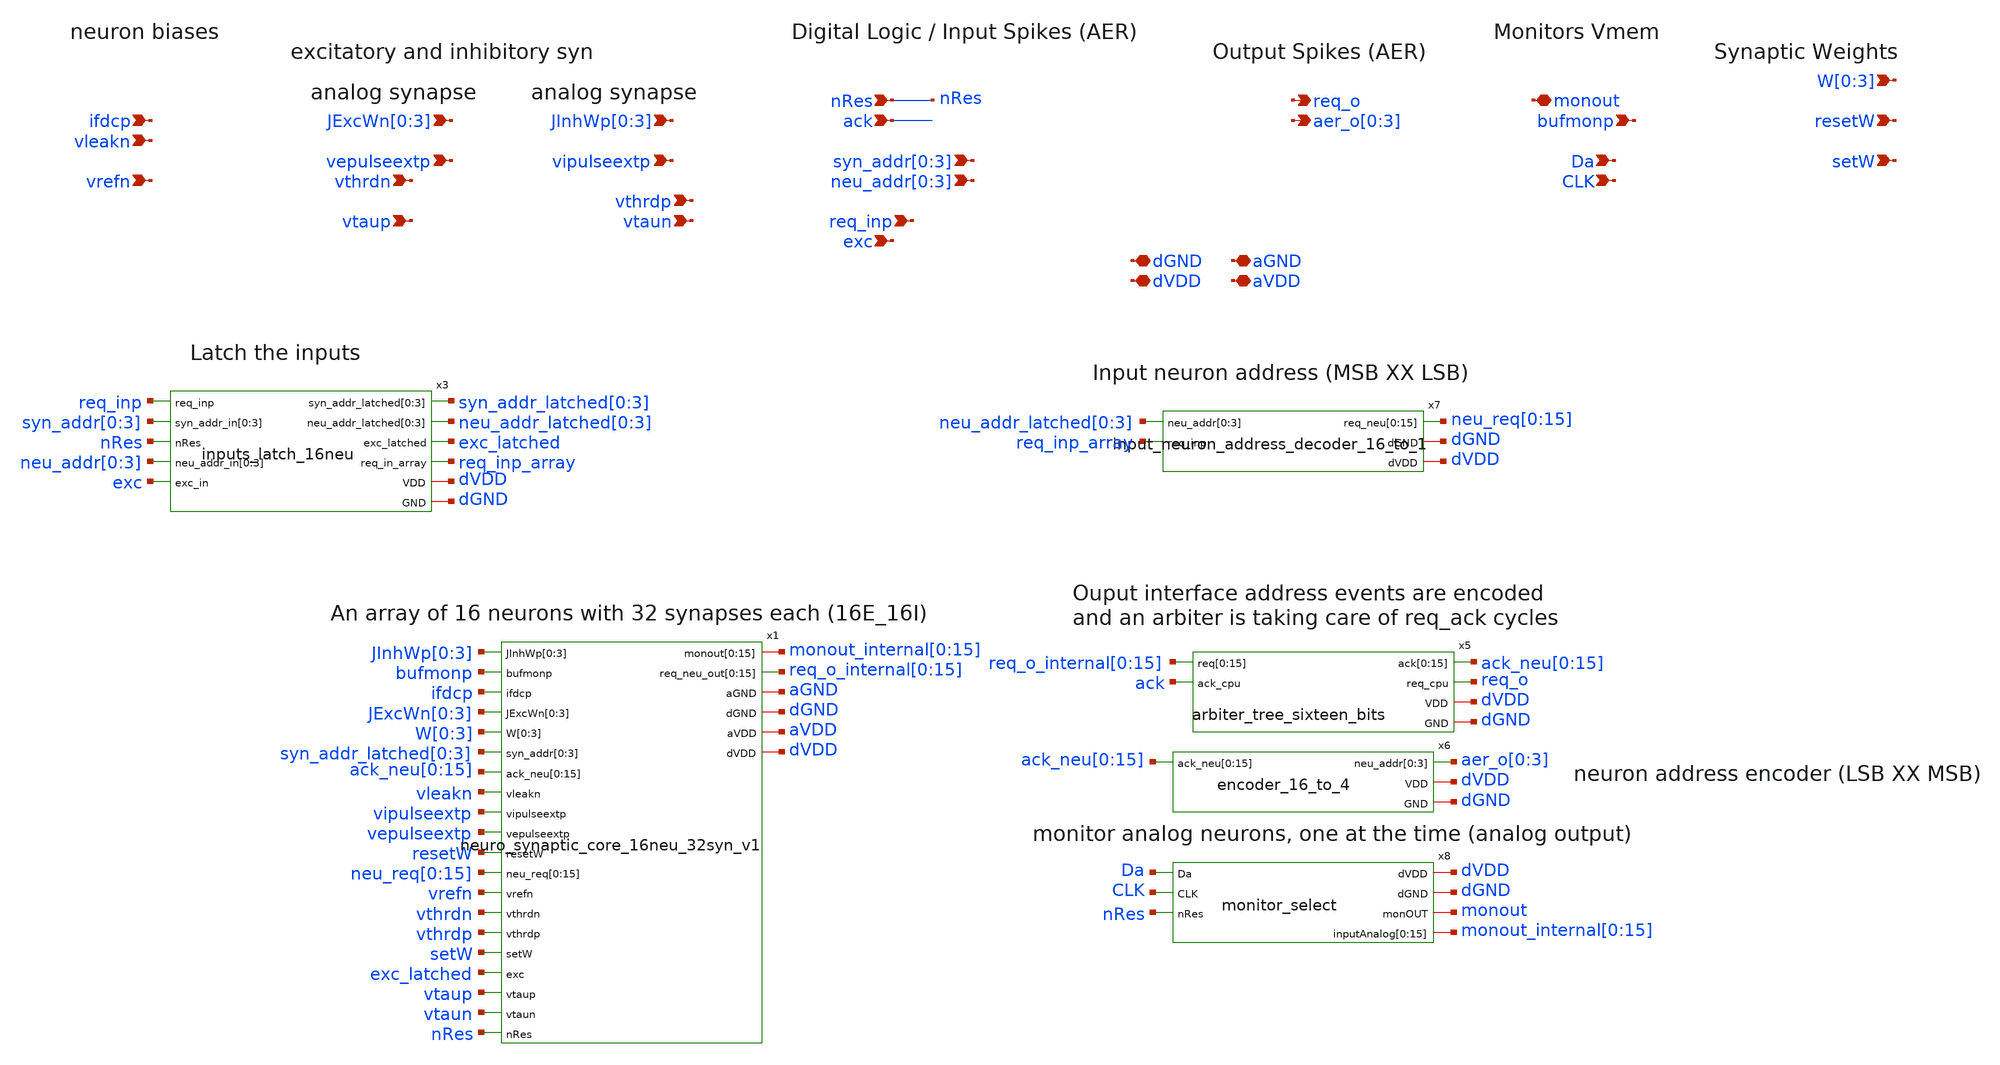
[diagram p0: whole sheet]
** sch_path: design/xschem/neuron_synapse_array_with_input_output_logic_v1.sch
**.subckt neuron_synapse_array_with_input_output_logic_v1 vleakn vrefn ifdcp bufmonp req_o
*+ aer_o[0],aer_o[1],aer_o[2],aer_o[3] dGND dVDD nRes ack neu_addr[0],neu_addr[1],neu_addr[2],neu_addr[3] req_inp
*+ syn_addr[0],syn_addr[1],syn_addr[2],syn_addr[3] exc aVDD monout W[0],W[1],W[2],W[3] resetW setW vepulseextp vipulseextp
*+ JExcWn[0],JExcWn[1],JExcWn[2],JExcWn[3] JInhWp[0],JInhWp[1],JInhWp[2],JInhWp[3] vthrdp vtaun vthrdn vtaup Da CLK aGND
*.ipin vleakn
*.ipin vrefn
*.ipin ifdcp
*.ipin bufmonp
*.opin req_o
*.opin aer_o[0],aer_o[1],aer_o[2],aer_o[3]
*.iopin dGND
*.iopin dVDD
*.ipin nRes
*.ipin ack
*.ipin neu_addr[0],neu_addr[1],neu_addr[2],neu_addr[3]
*.ipin req_inp
*.ipin syn_addr[0],syn_addr[1],syn_addr[2],syn_addr[3]
*.ipin exc
*.iopin aVDD
*.iopin monout
*.ipin W[0],W[1],W[2],W[3]
*.ipin resetW
*.ipin setW
*.ipin vepulseextp
*.ipin vipulseextp
*.ipin JExcWn[0],JExcWn[1],JExcWn[2],JExcWn[3]
*.ipin JInhWp[0],JInhWp[1],JInhWp[2],JInhWp[3]
*.ipin vthrdp
*.ipin vtaun
*.ipin vthrdn
*.ipin vtaup
*.ipin Da
*.ipin CLK
*.iopin aGND
x1 JInhWp[0] JInhWp[1] JInhWp[2] JInhWp[3] bufmonp ifdcp JExcWn[0] JExcWn[1] JExcWn[2] JExcWn[3]
+ W[0] W[1] W[2] W[3] syn_addr_latched[0] syn_addr_latched[1] syn_addr_latched[2] syn_addr_latched[3]
+ ack_neu[0] ack_neu[1] ack_neu[2] ack_neu[3] ack_neu[4] ack_neu[5] ack_neu[6] ack_neu[7] ack_neu[8] ack_neu[9]
+ ack_neu[10] ack_neu[11] ack_neu[12] ack_neu[13] ack_neu[14] ack_neu[15] vleakn vipulseextp vepulseextp
+ monout_internal[0] monout_internal[1] monout_internal[2] monout_internal[3] monout_internal[4] monout_internal[5]
+ monout_internal[6] monout_internal[7] monout_internal[8] monout_internal[9] monout_internal[10] monout_internal[11]
+ monout_internal[12] monout_internal[13] monout_internal[14] monout_internal[15] resetW neu_req[0] neu_req[1] neu_req[2]
+ neu_req[3] neu_req[4] neu_req[5] neu_req[6] neu_req[7] neu_req[8] neu_req[9] neu_req[10] neu_req[11]
+ neu_req[12] neu_req[13] neu_req[14] neu_req[15] vrefn req_o_internal[0] req_o_internal[1] req_o_internal[2]
+ req_o_internal[3] req_o_internal[4] req_o_internal[5] req_o_internal[6] req_o_internal[7] req_o_internal[8]
+ req_o_internal[9] req_o_internal[10] req_o_internal[11] req_o_internal[12] req_o_internal[13] req_o_internal[14]
+ req_o_internal[15] vthrdn vthrdp setW exc_latched vtaup vtaun aGND dGND aVDD dVDD nRes
+ neuro_synaptic_core_16neu_32syn_v1
x5 req_o_internal[0] req_o_internal[1] req_o_internal[2] req_o_internal[3] req_o_internal[4]
+ req_o_internal[5] req_o_internal[6] req_o_internal[7] req_o_internal[8] req_o_internal[9] req_o_internal[10]
+ req_o_internal[11] req_o_internal[12] req_o_internal[13] req_o_internal[14] req_o_internal[15] ack ack_neu[0]
+ ack_neu[1] ack_neu[2] ack_neu[3] ack_neu[4] ack_neu[5] ack_neu[6] ack_neu[7] ack_neu[8] ack_neu[9] ack_neu[10]
+ ack_neu[11] ack_neu[12] ack_neu[13] ack_neu[14] ack_neu[15] req_o dVDD dGND arbiter_tree_sixteen_bits
x6 aer_o[0] aer_o[1] aer_o[2] aer_o[3] ack_neu[0] ack_neu[1] ack_neu[2] ack_neu[3] ack_neu[4]
+ ack_neu[5] ack_neu[6] ack_neu[7] ack_neu[8] ack_neu[9] ack_neu[10] ack_neu[11] ack_neu[12] ack_neu[13]
+ ack_neu[14] ack_neu[15] dVDD dGND encoder_16_to_4
x3 req_inp syn_addr_latched[0] syn_addr_latched[1] syn_addr_latched[2] syn_addr_latched[3]
+ syn_addr[0] syn_addr[1] syn_addr[2] syn_addr[3] nRes neu_addr_latched[0] neu_addr_latched[1]
+ neu_addr_latched[2] neu_addr_latched[3] neu_addr[0] neu_addr[1] neu_addr[2] neu_addr[3] exc_latched exc req_inp_array
+ dVDD dGND inputs_latch_16neu
x8 dVDD Da CLK dGND nRes monout monout_internal[0] monout_internal[1] monout_internal[2]
+ monout_internal[3] monout_internal[4] monout_internal[5] monout_internal[6] monout_internal[7] monout_internal[8]
+ monout_internal[9] monout_internal[10] monout_internal[11] monout_internal[12] monout_internal[13] monout_internal[14]
+ monout_internal[15] monitor_select
x7 neu_addr_latched[0] neu_addr_latched[1] neu_addr_latched[2] neu_addr_latched[3] neu_req[0]
+ neu_req[1] neu_req[2] neu_req[3] neu_req[4] neu_req[5] neu_req[6] neu_req[7] neu_req[8] neu_req[9] neu_req[10]
+ neu_req[11] neu_req[12] neu_req[13] neu_req[14] neu_req[15] dGND dVDD req_inp_array
+ input_neuron_address_decoder_16_to_1
**.ends
.end
